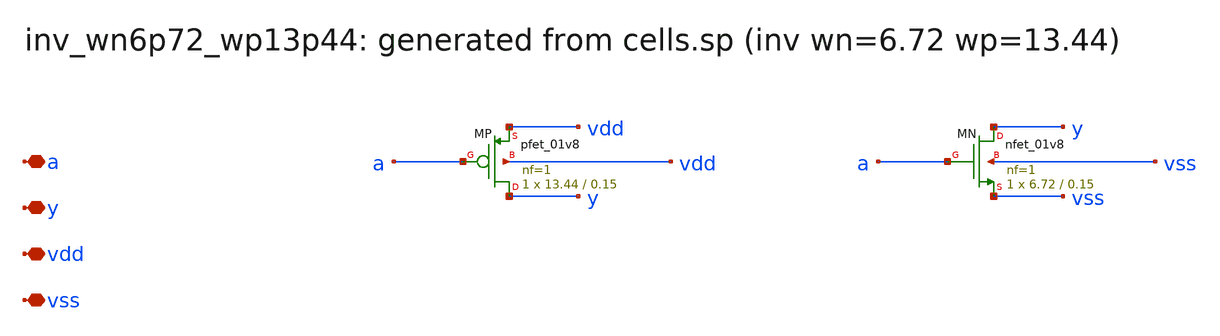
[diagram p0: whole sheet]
** sch_path: sram/xschem/inv_wn6p72_wp13p44.sch
**.subckt inv_wn6p72_wp13p44 a y vdd vss
*.iopin a
*.iopin y
*.iopin vdd
*.iopin vss
XMP y a vdd vdd sky130_fd_pr__pfet_01v8 L=0.15 W=13.44 nf=1 ad='int((nf+1)/2) * W/nf * 0.29' as='int((nf+2)/2) * W/nf * 0.29'
+ pd='2*int((nf+1)/2) * (W/nf + 0.29)' ps='2*int((nf+2)/2) * (W/nf + 0.29)' nrd='0.29 / W' nrs='0.29 / W'
+ sa=0 sb=0 sd=0 mult=1 m=1
XMN y a vss vss sky130_fd_pr__nfet_01v8 L=0.15 W=6.72 nf=1 ad='int((1 + 1)/2) * 6.72 / 1 * 0.29' as='int((1 + 2)/2) * 6.72 / 1 * 0.29'
+ pd='2*int((1 + 1)/2) * (6.72 / 1 + 0.29)' ps='2*int((1 + 2)/2) * (6.72 / 1 + 0.29)' nrd='0.29 / 6.72 '
+ nrs='0.29 / 6.72 ' sa=0 sb=0 sd=0 mult=1 m=1
**.ends
.end
